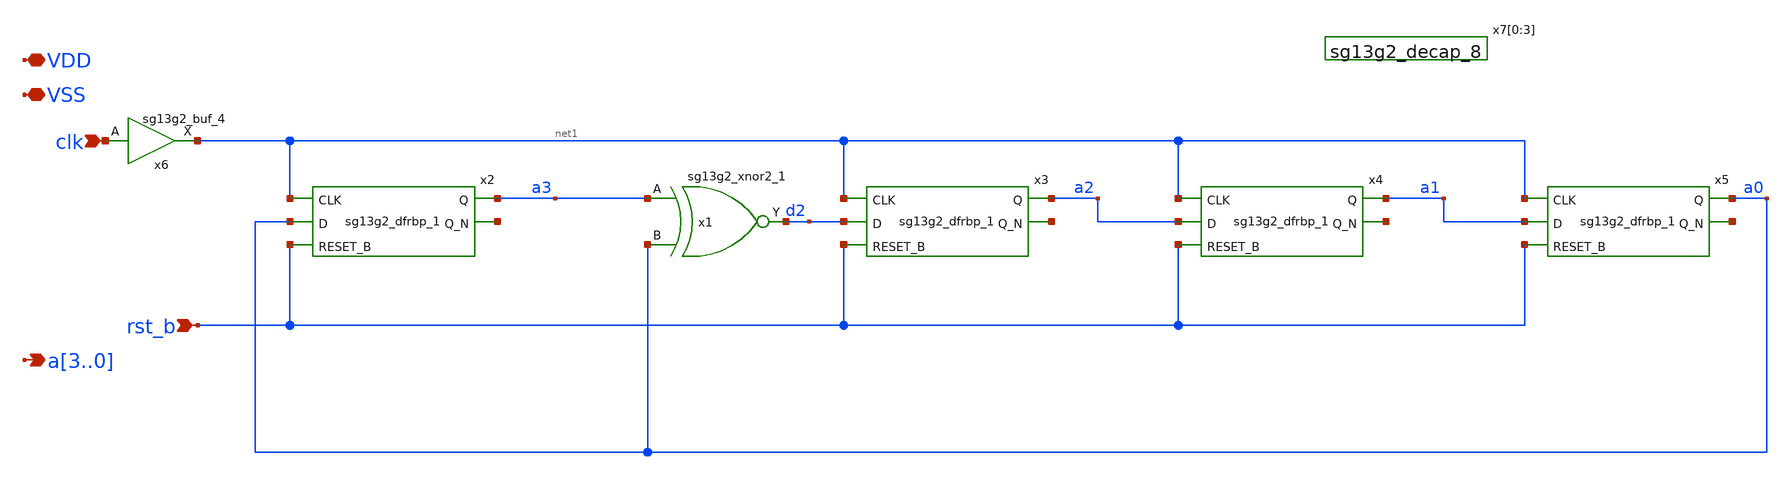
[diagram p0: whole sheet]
** sch_path: FLDO/design_data/xschem/lfsr4.sch
* IHP-GmbH/IHP-Open-PDK/ihp-sg13g2/libs.tech/xschem/sg13g2_stdcells/sg13g2_buf_4.sch:
* Copyright 2023 IHP PDK Authors
* Licensed under the Apache License, Version 2.0 (the "License");
**.subckt lfsr4 VDD clk VSS rst_b a3,a2,a1,a0
*.iopin VDD
*.ipin clk
*.iopin VSS
*.ipin rst_b
*.opin a3,a2,a1,a0
x1 d2 a3 a0 VDD VSS sg13g2_xnor2_1
x2 a3 net2 net1 a0 rst_b VDD VSS sg13g2_dfrbp_1
x3 a2 net3 net1 d2 rst_b VDD VSS sg13g2_dfrbp_1
x4 a1 net4 net1 a2 rst_b VDD VSS sg13g2_dfrbp_1
x5 a0 net5 net1 a1 rst_b VDD VSS sg13g2_dfrbp_1
x6 net1 clk VDD VSS sg13g2_buf_4
x7[0] VDD VSS sg13g2_decap_8
x7[1] VDD VSS sg13g2_decap_8
x7[2] VDD VSS sg13g2_decap_8
x7[3] VDD VSS sg13g2_decap_8
**.ends

* expanding   symbol:  sg13g2_stdcells/sg13g2_xnor2_1.sym # of pins=3
** sym_path: sg13g2_stdcells/sg13g2_xnor2_1.sym
** sch_path: sg13g2_stdcells/sg13g2_xnor2_1.sch
.subckt sg13g2_xnor2_1 Y A B VDD VSS
*.ipin A
*.opin Y
*.ipin B
*.iopin VDD
*.iopin VSS
XM1 net1 B net4 VSS sg13_lv_nmos w=640.00n l=130.00n ng=1 m=1 mm_ok=1
XM2 net4 A VSS VSS sg13_lv_nmos w=640.00n l=130.00n ng=1 m=1 mm_ok=1
XM3 net2 A VSS VSS sg13_lv_nmos w=740.00n l=130.00n ng=1 m=1 mm_ok=1
XM4 Y net1 net2 VSS sg13_lv_nmos w=740.00n l=130.00n ng=1 m=1 mm_ok=1
XM5 net2 B VSS VSS sg13_lv_nmos w=740.00n l=130.00n ng=1 m=1 mm_ok=1
XM6 net1 A VDD VDD sg13_lv_pmos w=840.00n l=130.00n ng=1 m=1 mm_ok=1
XM7 net1 B VDD VDD sg13_lv_pmos w=840.00n l=130.00n ng=1 m=1 mm_ok=1
XM8 net3 A VDD VDD sg13_lv_pmos w=1.12u l=130.00n ng=1 m=1 mm_ok=1
XM9 Y B net3 VDD sg13_lv_pmos w=1.12u l=130.00n ng=1 m=1 mm_ok=1
XM10 Y net1 VDD VDD sg13_lv_pmos w=1.12u l=130.00n ng=1 m=1 mm_ok=1
.ends


* expanding   symbol:  sg13g2_stdcells/sg13g2_dfrbp_1.sym # of pins=5
** sym_path: sg13g2_stdcells/sg13g2_dfrbp_1.sym
** sch_path: sg13g2_stdcells/sg13g2_dfrbp_1.sch
.subckt sg13g2_dfrbp_1 Q Q_N CLK D RESET_B VDD VSS
*.ipin D
*.ipin RESET_B
*.ipin CLK
*.opin Q
*.opin Q_N
*.iopin VDD
*.iopin VSS
XM1 Db D net10 VSS sg13_lv_nmos w=420.00n l=130.00n ng=1 m=1 mm_ok=1
XM2 net10 RESET_B VSS VSS sg13_lv_nmos w=420.00n l=130.00n ng=1 m=1 mm_ok=1
XM3 net1 clkneg net9 VSS sg13_lv_nmos w=420.00n l=130.00n ng=1 m=1 mm_ok=1
XM4 net9 net1 VSS VSS sg13_lv_nmos w=420.00n l=130.00n ng=1 m=1 mm_ok=1
XM5 net1 net1 net5 VSS sg13_lv_nmos w=420.00n l=130.00n ng=1 m=1 mm_ok=1
XM6 net5 RESET_B VSS VSS sg13_lv_nmos w=420.00n l=130.00n ng=1 m=1 mm_ok=1
XM7 Q_N net1 VSS VSS sg13_lv_nmos w=740.00n l=130.00n ng=1 m=1 mm_ok=1
XM8 net2 net1 VSS VSS sg13_lv_nmos w=740.00n l=130.00n ng=1 m=1 mm_ok=1
XM9 Q net2 VSS VSS sg13_lv_nmos w=740.00n l=130.00n ng=1 m=1 mm_ok=1
XM10 clkneg CLK VSS VSS sg13_lv_nmos w=740.00n l=130.00n ng=1 m=1 mm_ok=1
XM11 clkpos clkneg VSS VSS sg13_lv_nmos w=740.00n l=130.00n ng=1 m=1 mm_ok=1
XM12 Db clkneg net3 VSS sg13_lv_nmos w=420.00n l=130.00n ng=1 m=1 mm_ok=1
XM13 net3 clkpos net8 VSS sg13_lv_nmos w=420.00n l=130.00n ng=1 m=1 mm_ok=1
XM14 net8 net3 net4 VSS sg13_lv_nmos w=420.00n l=130.00n ng=1 m=1 mm_ok=1
XM15 net4 RESET_B VSS VSS sg13_lv_nmos w=420.00n l=130.00n ng=1 m=1 mm_ok=1
XM16 net3 net3 VSS VSS sg13_lv_nmos w=740.00n l=130.00n ng=1 m=1 mm_ok=1
XM17 net3 clkpos net1 VSS sg13_lv_nmos w=740.00n l=130.00n ng=1 m=1 mm_ok=1
XM18 Db RESET_B VDD VDD sg13_lv_pmos w=420.00n l=130.00n ng=1 m=1 mm_ok=1
XM19 Db D VDD VDD sg13_lv_pmos w=420.00n l=130.00n ng=1 m=1 mm_ok=1
XM20 net7 net1 VDD VDD sg13_lv_pmos w=420.00n l=130.00n ng=1 m=1 mm_ok=1
XM21 net1 clkpos net7 VDD sg13_lv_pmos w=420.00n l=130.00n ng=1 m=1 mm_ok=1
XM22 net1 net1 VDD VDD sg13_lv_pmos w=420.00n l=130.00n ng=1 m=1 mm_ok=1
XM23 net1 RESET_B VDD VDD sg13_lv_pmos w=420.00n l=130.00n ng=1 m=1 mm_ok=1
XM24 Q_N net1 VDD VDD sg13_lv_pmos w=1.12u l=130.00n ng=1 m=1 mm_ok=1
XM25 net2 net1 VDD VDD sg13_lv_pmos w=1.12u l=130.00n ng=1 m=1 mm_ok=1
XM26 Q net2 VDD VDD sg13_lv_pmos w=1.12u l=130.00n ng=1 m=1 mm_ok=1
XM27 clkneg CLK VDD VDD sg13_lv_pmos w=1.12u l=130.00n ng=1 m=1 mm_ok=1
XM28 clkpos clkneg VDD VDD sg13_lv_pmos w=1.12u l=130.00n ng=1 m=1 mm_ok=1
XM29 Db clkpos net3 VDD sg13_lv_pmos w=420.00n l=130.00n ng=1 m=1 mm_ok=1
XM30 net6 net3 VDD VDD sg13_lv_pmos w=420.00n l=130.00n ng=1 m=1 mm_ok=1
XM31 net3 clkneg net6 VDD sg13_lv_pmos w=420.00n l=130.00n ng=1 m=1 mm_ok=1
XM32 net3 RESET_B VDD VDD sg13_lv_pmos w=420.00n l=130.00n ng=1 m=1 mm_ok=1
XM33 net3 net3 VDD VDD sg13_lv_pmos w=1.000u l=130.00n ng=1 m=1 mm_ok=1
XM34 net3 clkneg net1 VDD sg13_lv_pmos w=1.000u l=130.00n ng=1 m=1 mm_ok=1
.ends


* expanding   symbol:  sg13g2_stdcells/sg13g2_buf_4.sym # of pins=2
** sym_path: sg13g2_stdcells/sg13g2_buf_4.sym
** sch_path: sg13g2_stdcells/sg13g2_buf_4.sch
.subckt sg13g2_buf_4 X A VDD VSS
*.ipin A
*.opin X
*.iopin VDD
*.iopin VSS
XM1 net1 A VSS VSS sg13_lv_nmos w=740.00n l=130.00n ng=1 m=1 mm_ok=1
XM2 X net1 VSS VSS sg13_lv_nmos w=2.96u l=130.00n ng=4 m=1 mm_ok=1
XM3 net1 A VDD VDD sg13_lv_pmos w=1.68u l=130.00n ng=2 m=1 mm_ok=1
XM4 X net1 VDD VDD sg13_lv_pmos w=4.48u l=130.00n ng=4 m=1 mm_ok=1
.ends


* expanding   symbol:  sg13g2_stdcells/sg13g2_decap_8.sym # of pins=0
** sym_path: sg13g2_stdcells/sg13g2_decap_8.sym
** sch_path: sg13g2_stdcells/sg13g2_decap_8.sch
.subckt sg13g2_decap_8 VDD VSS
*.iopin VDD
*.iopin VSS
XM1 VSS VDD VSS VSS sg13_lv_nmos w=840.00n l=1.000u ng=2 m=1 mm_ok=1
XM2 VDD VSS VDD VDD sg13_lv_pmos w=2.000u l=1.000u ng=2 m=1 mm_ok=1
.ends

.end
